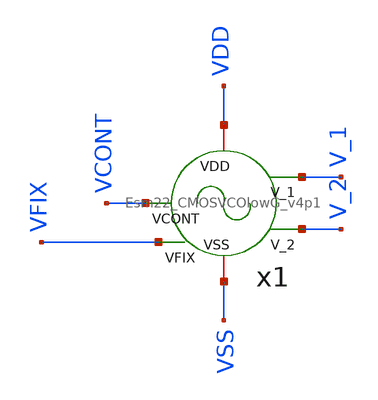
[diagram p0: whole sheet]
** sch_path: xschem/tb_CMOSVCO_v4p1.sch
.lib $::SKYWATER_MODELS/sky130.lib.spice tt
.include $::SKYWATER_STDCELLS/sky130_fd_sc_hd.spice

**.subckt tb_CMOSVCO_v4p1
x1 VCONT VSS VDD V_1 V_2 VFIX Esm22_CMOSVCOlowG_v4p1
**** begin user architecture code

vvdd vdd 0 dc 3.3
vvss vss 0 0
vvcont VCONT 0 dc 1.65
vvfix VFIX 0 dc 1
*.option temp = 200
.ic v(V_1) = 0
.ic v(V_2) = 3.3

.control
   compose vin_var start=0.1 stop=2 step=0.1
   foreach val $&vin_var
     alter vvcont $val
     tran 5n 300u
   end
wrdata /foss/designs/TO202406_CMOSVCO_Esm22/xschem/data/data_CMOSVCOlowG_v4p1.txt v(V_1)
+ tran1.v(V_1) tran2.v(V_1) tran3.v(V_1) tran4.v(V_1) tran5.v(V_1) tran6.v(V_1) tran7.v(V_1) tran8.v(V_1)
+ tran9.v(V_1) tran10.v(V_1) tran11.v(V_1) tran12.v(V_1) tran13.v(V_1) tran14.v(V_1) tran15.v(V_1) tran16.v(V_1)
+ tran17.v(V_1) tran18.v(V_1) tran19.v(V_1)
plot tran1.v(V_1) (tran10.v(V_1)+4) (tran19.v(V_1)+8)
.endc


**** end user architecture code
**.ends
.end
